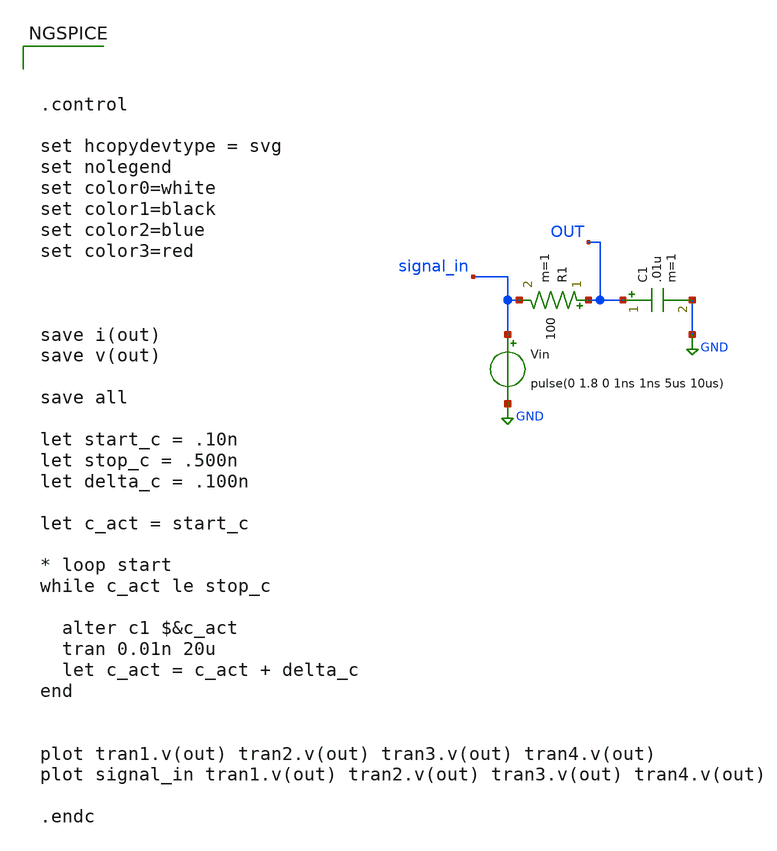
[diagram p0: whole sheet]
** sch_path: exp/SKY130/sweep_params/RC_sweep.sch
**.subckt RC_sweep
R1 OUT signal_in 100 m=1
C1 OUT GND .01u m=1
Vin signal_in GND pulse(0 1.8 0 1ns 1ns 5us 10us)
**** begin user architecture code

** opencircuitdesign pdks install
.lib $::SKYWATER_MODELS/sky130.lib.spice tt





.control

set hcopydevtype = svg
set nolegend
set color0=white
set color1=black
set color2=blue
set color3=red



save i(out)
save v(out)

save all

let start_c = .10n
let stop_c = .500n
let delta_c = .100n

let c_act = start_c

* loop start
while c_act le stop_c

  alter c1 $&c_act
  tran 0.01n 20u
  let c_act = c_act + delta_c
end


plot tran1.v(out) tran2.v(out) tran3.v(out) tran4.v(out)
plot signal_in tran1.v(out) tran2.v(out) tran3.v(out) tran4.v(out)

.endc



**** end user architecture code
**.ends
.GLOBAL GND
.end
